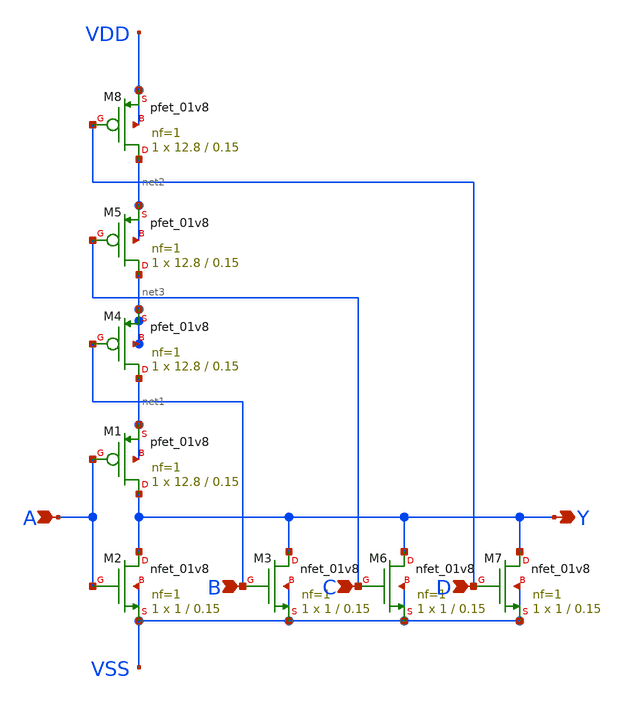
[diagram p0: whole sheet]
** sch_path: design/xschem/NOR/nor4.sch
**.subckt nor4 A Y B C D
*.ipin A
*.opin Y
*.ipin B
*.ipin C
*.ipin D
XM1 Y A net1 net1 sky130_fd_pr__pfet_01v8 L=0.15 W=12.8 nf=1 ad='int((nf+1)/2) * W/nf * 0.29' as='int((nf+2)/2) * W/nf * 0.29'
+ pd='2*int((nf+1)/2) * (W/nf + 0.29)' ps='2*int((nf+2)/2) * (W/nf + 0.29)' nrd='0.29 / W' nrs='0.29 / W'
+ sa=0 sb=0 sd=0 mult=1 m=1
XM2 Y A VSS VSS sky130_fd_pr__nfet_01v8 L=0.15 W=1 nf=1 ad='int((nf+1)/2) * W/nf * 0.29' as='int((nf+2)/2) * W/nf * 0.29'
+ pd='2*int((nf+1)/2) * (W/nf + 0.29)' ps='2*int((nf+2)/2) * (W/nf + 0.29)' nrd='0.29 / W' nrs='0.29 / W'
+ sa=0 sb=0 sd=0 mult=1 m=1
XM3 Y B VSS VSS sky130_fd_pr__nfet_01v8 L=0.15 W=1 nf=1 ad='int((nf+1)/2) * W/nf * 0.29' as='int((nf+2)/2) * W/nf * 0.29'
+ pd='2*int((nf+1)/2) * (W/nf + 0.29)' ps='2*int((nf+2)/2) * (W/nf + 0.29)' nrd='0.29 / W' nrs='0.29 / W'
+ sa=0 sb=0 sd=0 mult=1 m=1
XM4 net1 B net3 net3 sky130_fd_pr__pfet_01v8 L=0.15 W=12.8 nf=1 ad='int((nf+1)/2) * W/nf * 0.29' as='int((nf+2)/2) * W/nf * 0.29'
+ pd='2*int((nf+1)/2) * (W/nf + 0.29)' ps='2*int((nf+2)/2) * (W/nf + 0.29)' nrd='0.29 / W' nrs='0.29 / W'
+ sa=0 sb=0 sd=0 mult=1 m=1
XM5 net3 C net2 net2 sky130_fd_pr__pfet_01v8 L=0.15 W=12.8 nf=1 ad='int((nf+1)/2) * W/nf * 0.29' as='int((nf+2)/2) * W/nf * 0.29'
+ pd='2*int((nf+1)/2) * (W/nf + 0.29)' ps='2*int((nf+2)/2) * (W/nf + 0.29)' nrd='0.29 / W' nrs='0.29 / W'
+ sa=0 sb=0 sd=0 mult=1 m=1
XM6 Y C VSS VSS sky130_fd_pr__nfet_01v8 L=0.15 W=1 nf=1 ad='int((nf+1)/2) * W/nf * 0.29' as='int((nf+2)/2) * W/nf * 0.29'
+ pd='2*int((nf+1)/2) * (W/nf + 0.29)' ps='2*int((nf+2)/2) * (W/nf + 0.29)' nrd='0.29 / W' nrs='0.29 / W'
+ sa=0 sb=0 sd=0 mult=1 m=1
XM7 Y D VSS VSS sky130_fd_pr__nfet_01v8 L=0.15 W=1 nf=1 ad='int((nf+1)/2) * W/nf * 0.29' as='int((nf+2)/2) * W/nf * 0.29'
+ pd='2*int((nf+1)/2) * (W/nf + 0.29)' ps='2*int((nf+2)/2) * (W/nf + 0.29)' nrd='0.29 / W' nrs='0.29 / W'
+ sa=0 sb=0 sd=0 mult=1 m=1
XM8 net2 D VDD VDD sky130_fd_pr__pfet_01v8 L=0.15 W=12.8 nf=1 ad='int((nf+1)/2) * W/nf * 0.29' as='int((nf+2)/2) * W/nf * 0.29'
+ pd='2*int((nf+1)/2) * (W/nf + 0.29)' ps='2*int((nf+2)/2) * (W/nf + 0.29)' nrd='0.29 / W' nrs='0.29 / W'
+ sa=0 sb=0 sd=0 mult=1 m=1
**.ends
.end
